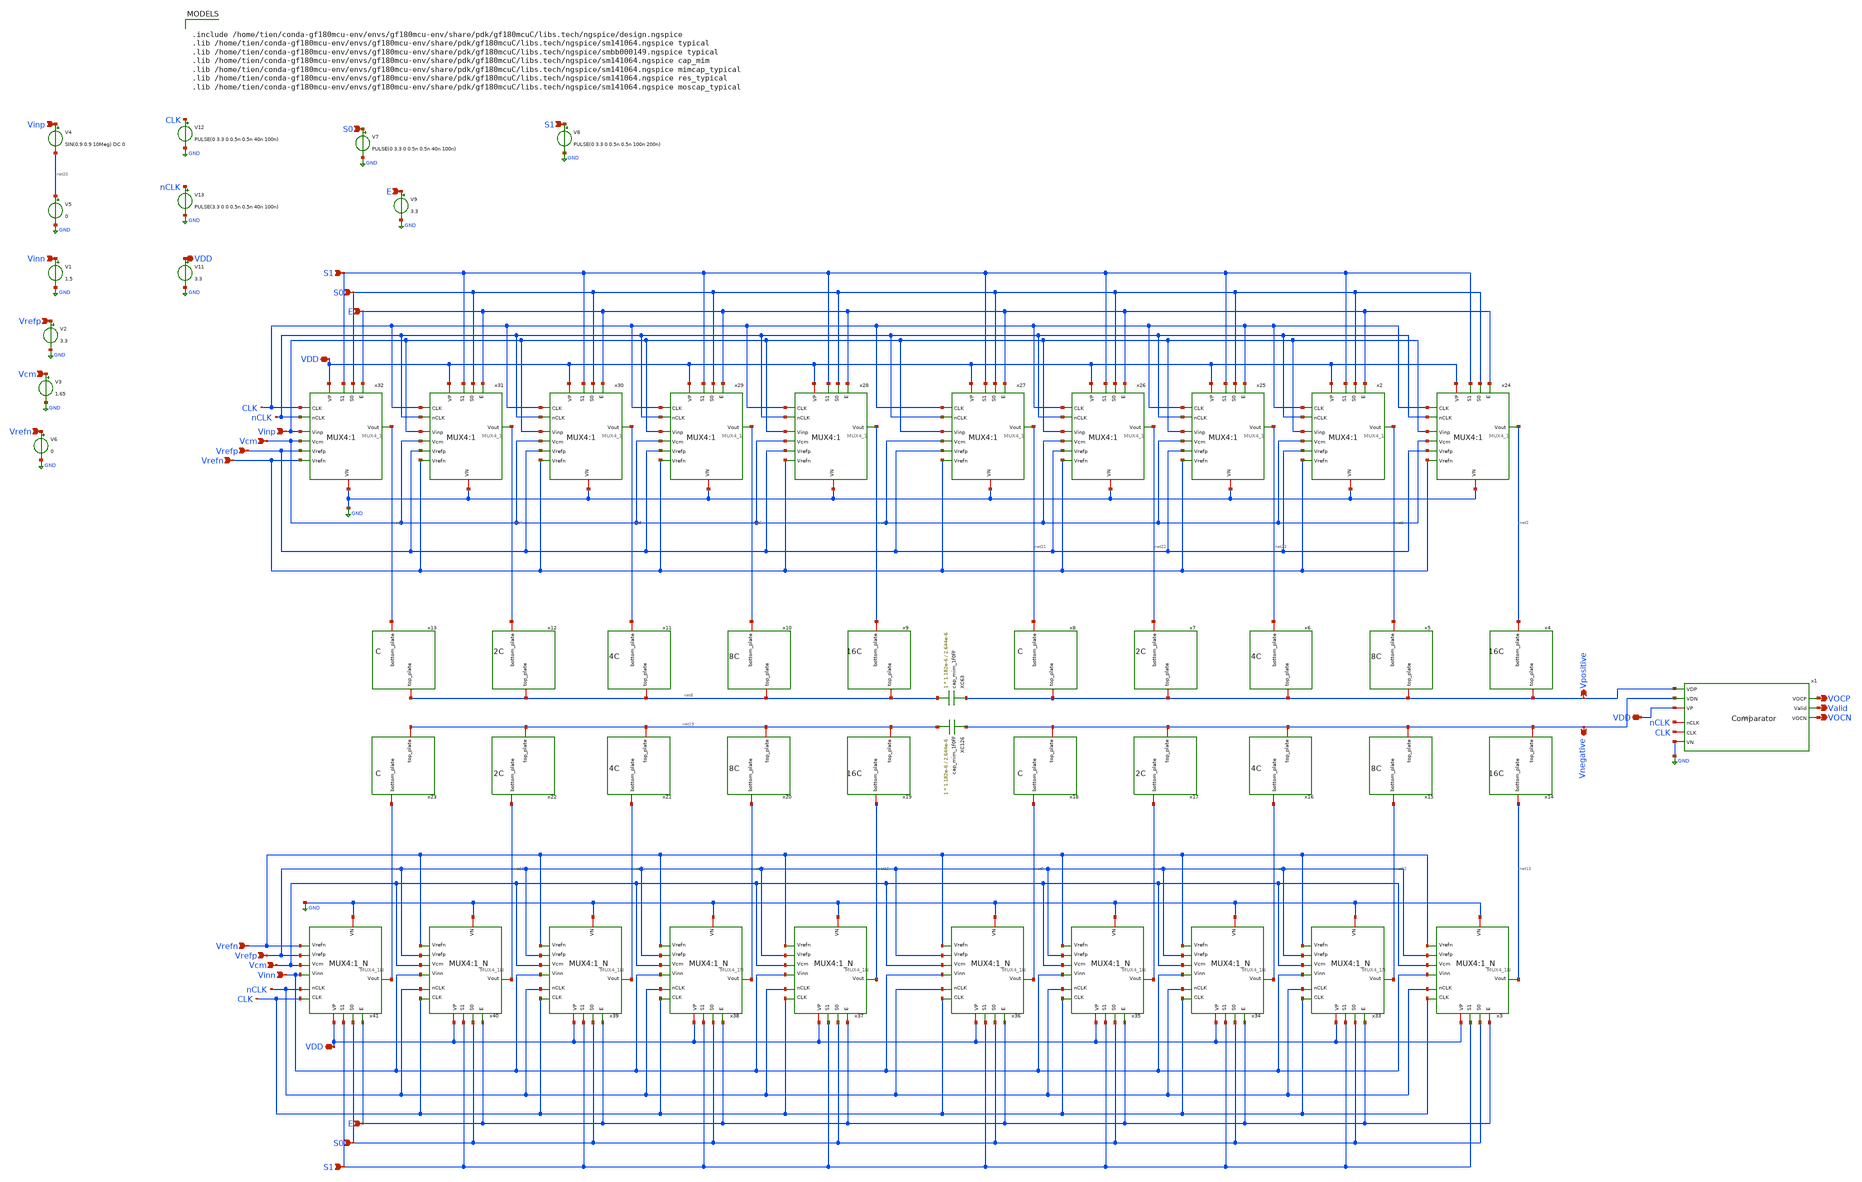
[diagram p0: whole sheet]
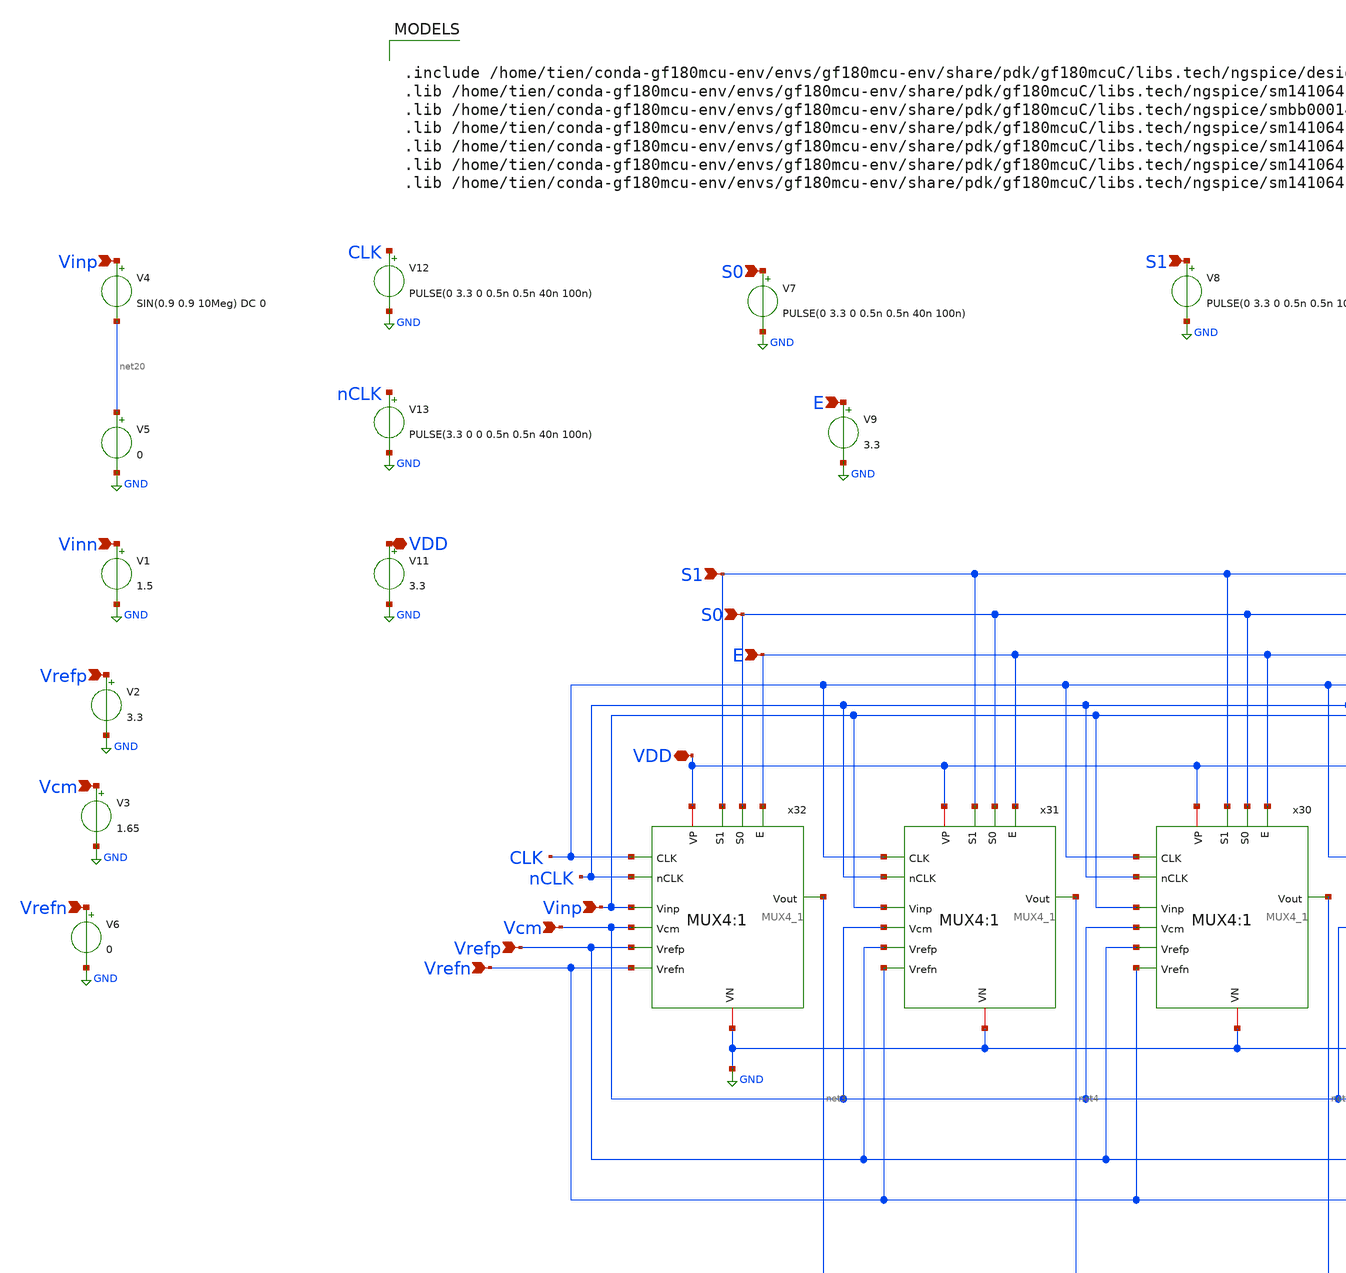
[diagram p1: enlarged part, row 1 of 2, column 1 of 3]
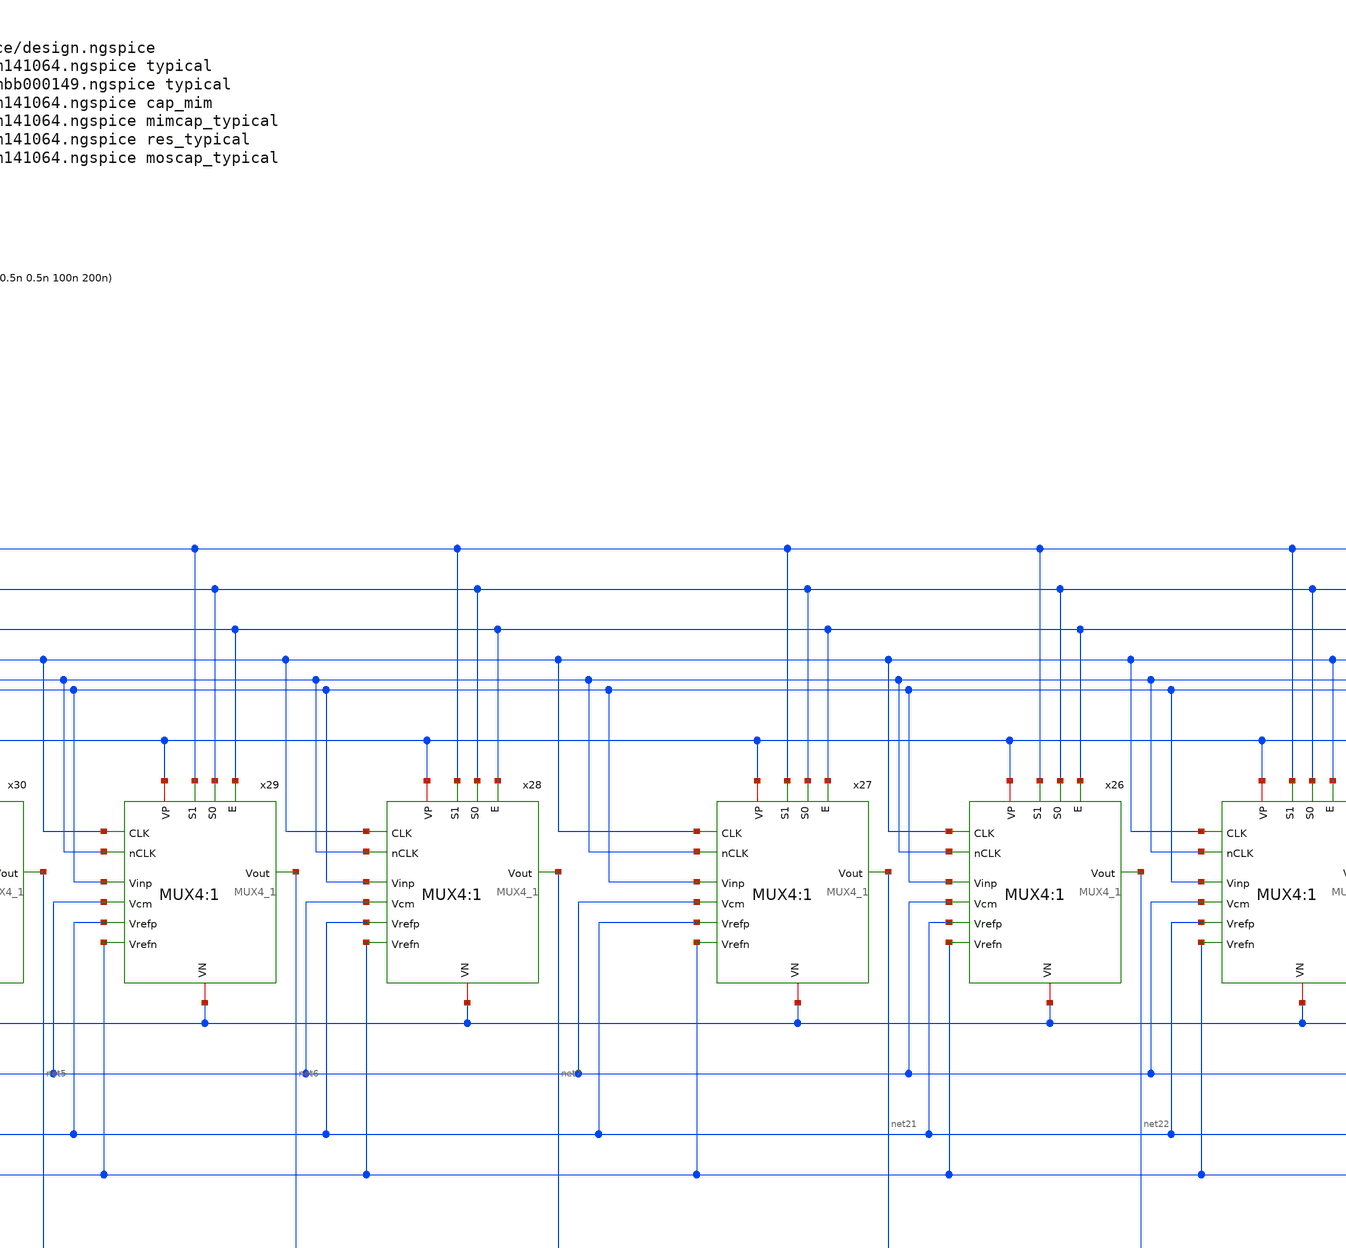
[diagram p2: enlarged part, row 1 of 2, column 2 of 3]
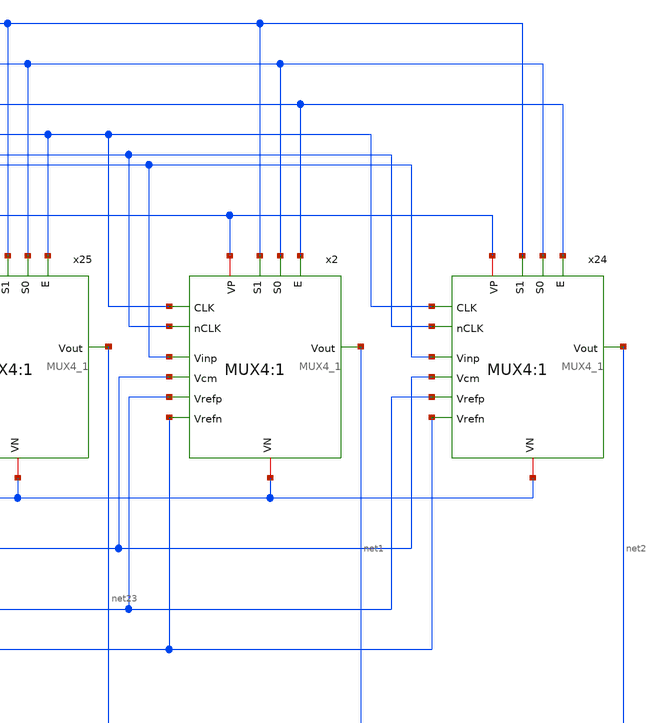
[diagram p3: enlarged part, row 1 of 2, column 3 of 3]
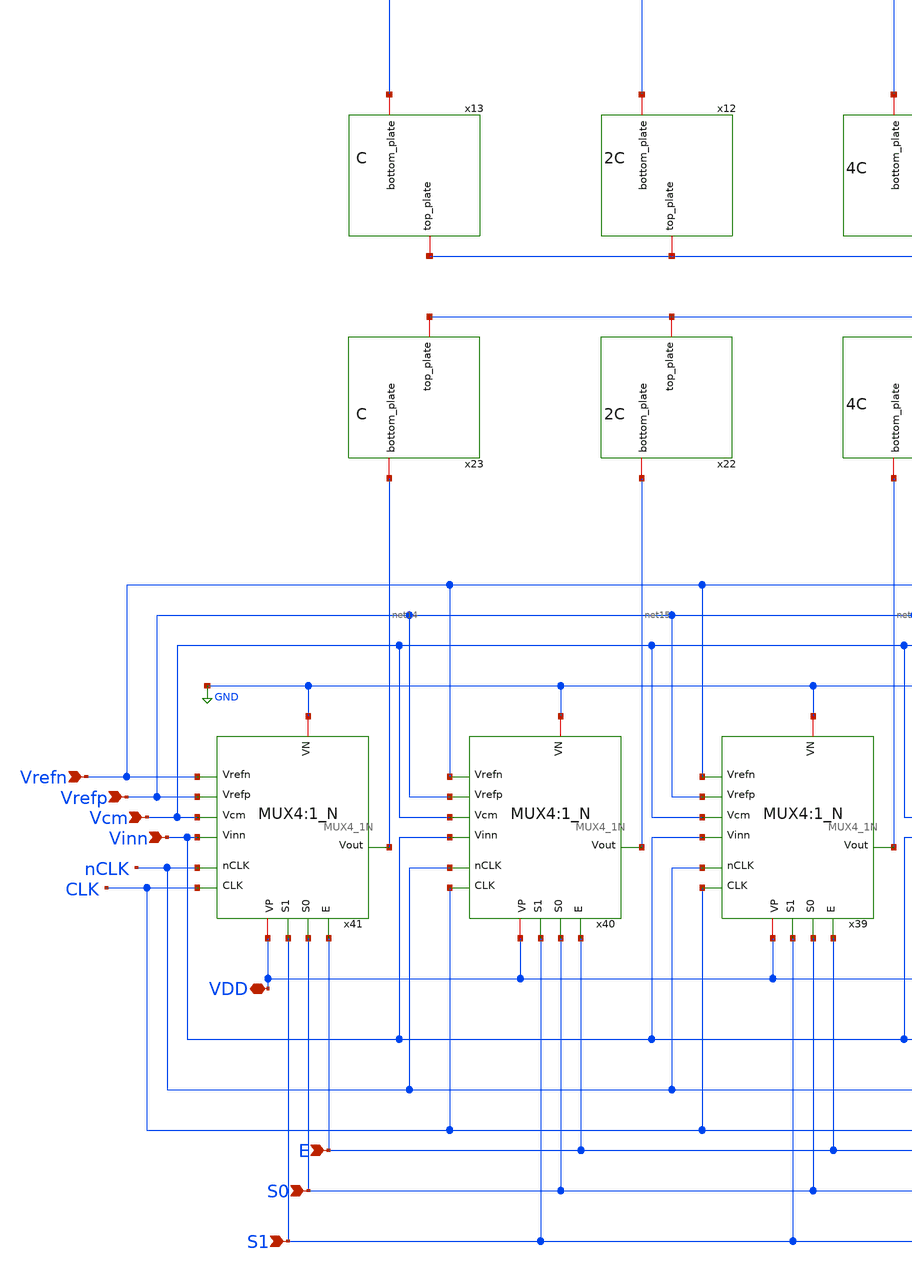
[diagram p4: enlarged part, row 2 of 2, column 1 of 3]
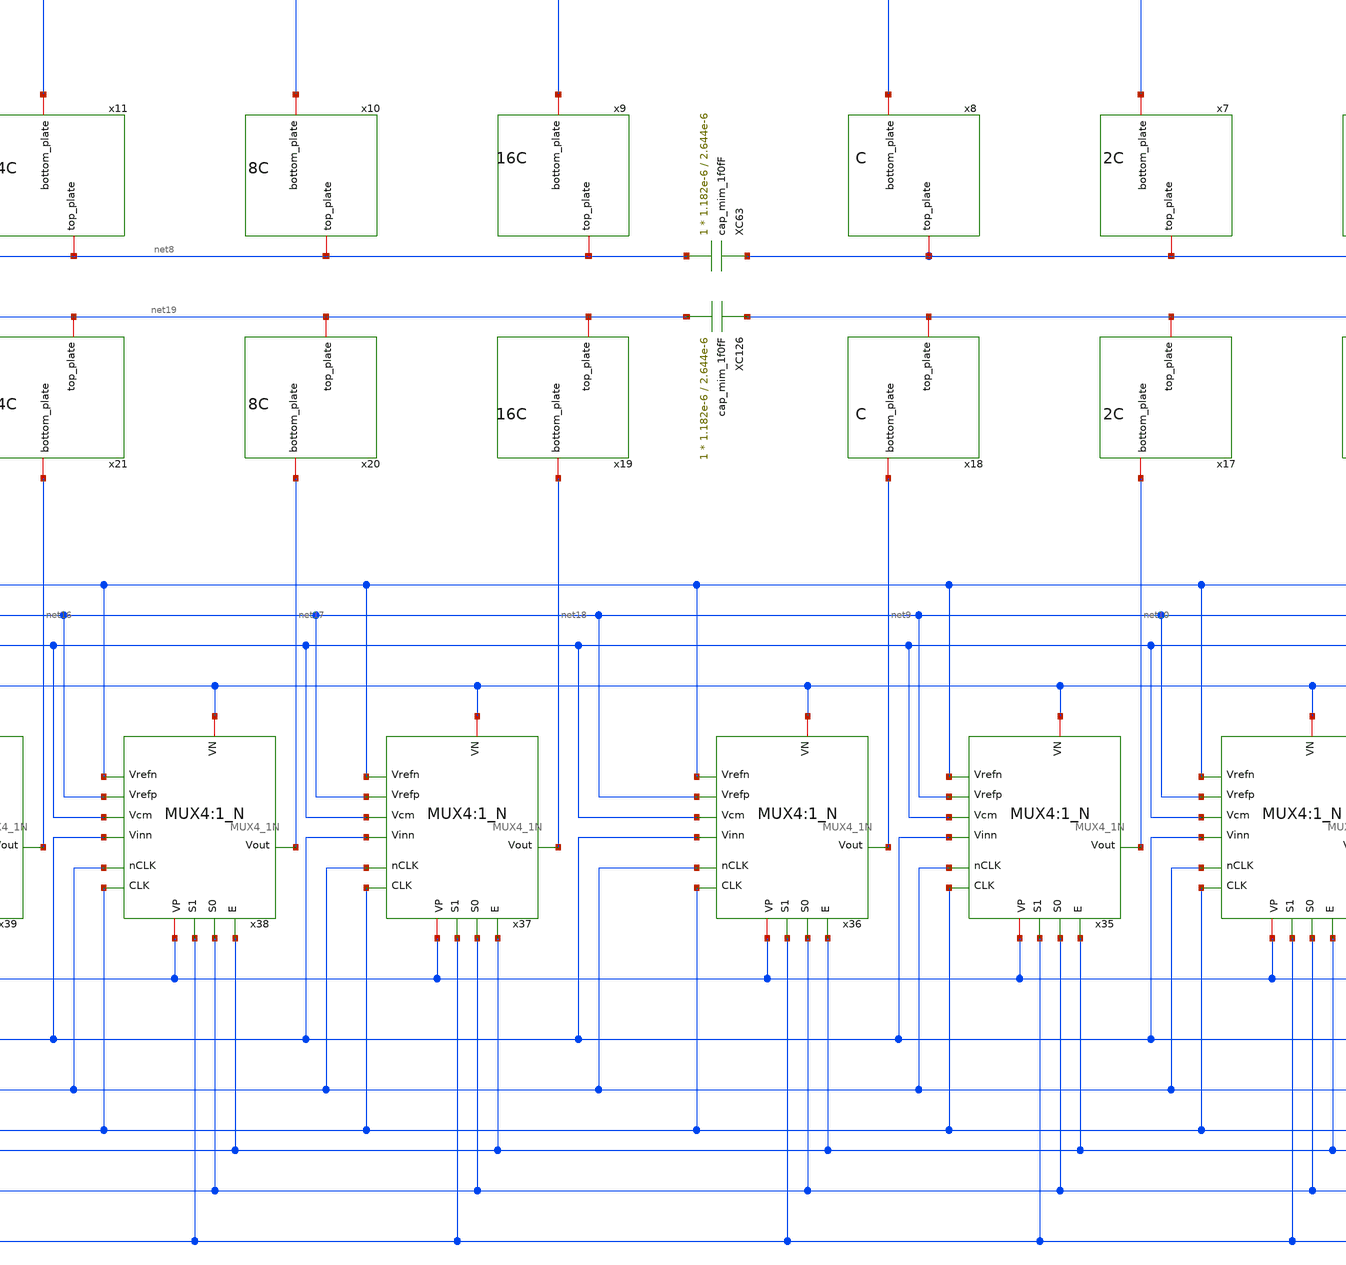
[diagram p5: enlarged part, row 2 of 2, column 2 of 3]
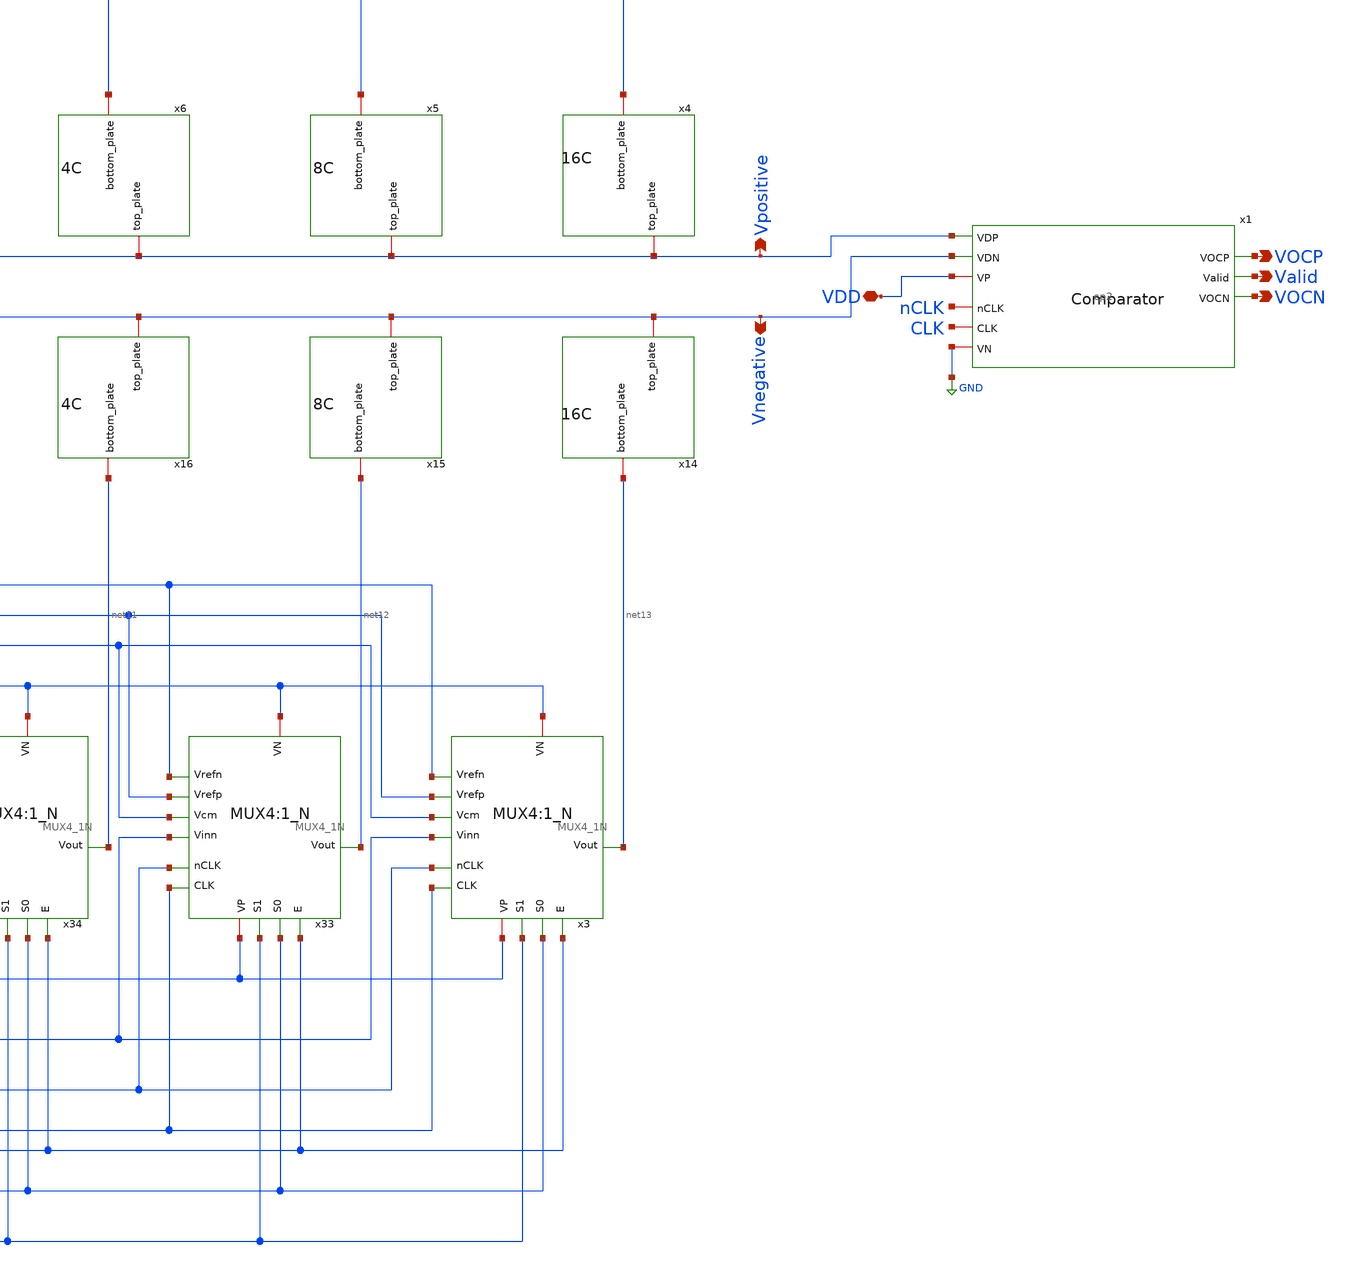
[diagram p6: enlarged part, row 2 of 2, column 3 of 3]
** sch_path: CDAC/ADC_SAR.sch
**.subckt ADC_SAR Valid VOCP VOCN Vinp Vinn VDD Vinp S1 Vpositive Vnegative Vcm Vrefp Vrefn Vrefn
*+ Vrefp Vcm Vrefp Vcm Vrefn S0 E Vinn S1 S0 E VDD VDD VDD S1 S0 E
*.opin Valid
*.opin VOCP
*.opin VOCN
*.ipin Vinp
*.ipin Vinn
*.iopin VDD
*.ipin Vinp
*.ipin S1
*.opin Vpositive
*.opin Vnegative
*.ipin Vcm
*.ipin Vrefp
*.ipin Vrefn
*.ipin Vrefn
*.ipin Vrefp
*.ipin Vcm
*.ipin Vrefp
*.ipin Vcm
*.ipin Vrefn
*.ipin S0
*.ipin E
*.ipin Vinn
*.ipin S1
*.ipin S0
*.ipin E
*.iopin VDD
*.iopin VDD
*.iopin VDD
*.ipin S1
*.ipin S0
*.ipin E
x1 VDD VOCP Vpositive Vnegative Valid VOCN nCLK CLK GND cp2
XC63 Vpositive net8 cap_mim_1f0fF c_width=1.182e-6 c_length=2.644e-6 m=1
XC126 Vnegative net19 cap_mim_1f0fF c_width=1.182e-6 c_length=2.644e-6 m=1
x4 net2 Vpositive 16C
x5 Vpositive net1 8C
x6 net23 Vpositive 4C
x7 net22 Vpositive 2C
x8 net21 Vpositive C
x9 net7 net8 16C
x10 net8 net6 8C
x11 net5 net8 4C
x12 net4 net8 2C
x13 net3 net8 C
x14 net13 Vnegative 16C
x15 Vnegative net12 8C
x16 net11 Vnegative 4C
x17 net10 Vnegative 2C
x18 net9 Vnegative C
x19 net18 net19 16C
x20 net19 net17 8C
x21 net16 net19 4C
x22 net15 net19 2C
x23 net14 net19 C
V11 VDD GND 3.3
V12 CLK GND PULSE(0 3.3 0 0.5n 0.5n 40n 100n)

V13 nCLK GND PULSE(3.3 0 0 0.5n 0.5n 40n 100n)

V4 Vinp net20 SIN(0.9 0.9 10Meg) DC 0
V5 net20 GND 0
V1 Vinn GND 1.5
x24 VDD Vinp E CLK nCLK Vcm net2 Vrefp Vrefn S0 S1 GND MUX4_1
x2 VDD Vinp E CLK nCLK Vcm net1 Vrefp Vrefn S0 S1 GND MUX4_1
x25 VDD Vinp CLK CLK nCLK Vcm net23 Vrefp Vrefn S0 S1 GND MUX4_1
x26 VDD Vinp E CLK nCLK Vcm net22 Vrefp Vrefn S0 S1 GND MUX4_1
x27 VDD Vinp E CLK nCLK Vcm net21 Vrefp Vrefn S0 S1 GND MUX4_1
x28 VDD Vinp E CLK nCLK Vcm net7 Vrefp Vrefn S0 S1 GND MUX4_1
x29 VDD Vinp E CLK nCLK Vcm net6 Vrefp Vrefn S0 S1 GND MUX4_1
x30 VDD Vinp E CLK nCLK Vcm net5 Vrefp Vrefn S0 S1 GND MUX4_1
x31 VDD Vinp E CLK nCLK Vcm net4 Vrefp Vrefn S0 S1 GND MUX4_1
x32 VDD Vinp E CLK nCLK Vcm net3 Vrefp Vrefn S0 S1 GND MUX4_1
x3 VDD Vinn E CLK nCLK Vcm net13 Vrefp Vrefn S0 S1 GND MUX4_1N
x33 VDD Vinn E CLK nCLK Vcm net12 Vrefp Vrefn S0 S1 GND MUX4_1N
x34 VDD Vinn E CLK nCLK Vcm net11 Vrefp Vrefn S0 S1 GND MUX4_1N
x35 VDD Vinn E CLK nCLK Vcm net10 Vrefp Vrefn S0 S1 GND MUX4_1N
x36 VDD Vinn E CLK nCLK Vcm net9 Vrefp Vrefn S0 S1 GND MUX4_1N
x37 VDD Vinn E CLK nCLK Vcm net18 Vrefp Vrefn S0 S1 GND MUX4_1N
x38 VDD Vinn E CLK nCLK Vcm net17 Vrefp Vrefn S0 S1 GND MUX4_1N
x39 VDD Vinn E CLK nCLK Vcm net16 Vrefp Vrefn S0 S1 GND MUX4_1N
x40 VDD Vinn E CLK nCLK Vcm net15 Vrefp Vrefn S0 S1 GND MUX4_1N
x41 VDD Vinn E CLK nCLK Vcm net14 Vrefp Vrefn S0 S1 GND MUX4_1N
V2 Vrefp GND 3.3
V3 Vcm GND 1.65
V6 Vrefn GND 0
V7 S0 GND PULSE(0 3.3 0 0.5n 0.5n 40n 100n)


V8 S1 GND PULSE(0 3.3 0 0.5n 0.5n 100n 200n)

V9 E GND 3.3
**** begin user architecture code

.tran 0.01n 1u
.temp 25
.save all



.include /home/tien/conda-gf180mcu-env/envs/gf180mcu-env/share/pdk/gf180mcuC/libs.tech/ngspice/design.ngspice
.lib /home/tien/conda-gf180mcu-env/envs/gf180mcu-env/share/pdk/gf180mcuC/libs.tech/ngspice/sm141064.ngspice typical
.lib /home/tien/conda-gf180mcu-env/envs/gf180mcu-env/share/pdk/gf180mcuC/libs.tech/ngspice/smbb000149.ngspice typical
.lib /home/tien/conda-gf180mcu-env/envs/gf180mcu-env/share/pdk/gf180mcuC/libs.tech/ngspice/sm141064.ngspice cap_mim
.lib /home/tien/conda-gf180mcu-env/envs/gf180mcu-env/share/pdk/gf180mcuC/libs.tech/ngspice/sm141064.ngspice mimcap_typical
.lib /home/tien/conda-gf180mcu-env/envs/gf180mcu-env/share/pdk/gf180mcuC/libs.tech/ngspice/sm141064.ngspice res_typical
.lib /home/tien/conda-gf180mcu-env/envs/gf180mcu-env/share/pdk/gf180mcuC/libs.tech/ngspice/sm141064.ngspice moscap_typical

**** end user architecture code
**.ends
.GLOBAL GND
.end
